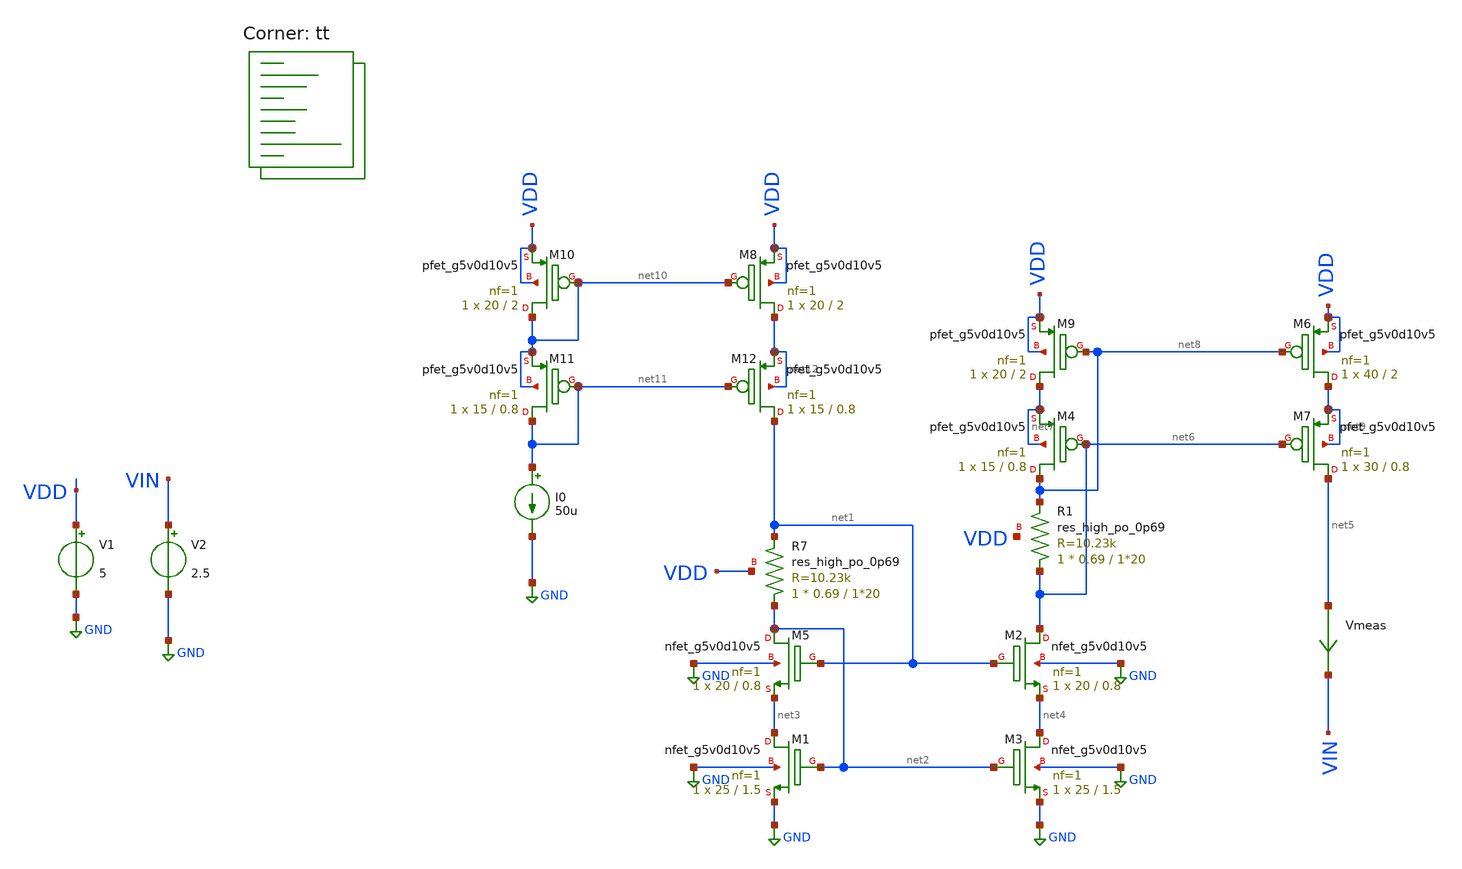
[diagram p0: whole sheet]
** sch_path: old stuff/folded_cascode_amplifier_upgraded/Low_voltage_current_mirror_NMOS/circ_test.sch
**.subckt circ_test
V1 VDD GND 5
V2 VIN GND 2.5
XR7 net2 net1 VDD sky130_fd_pr__res_high_po_0p69 L=1*20 mult=1 m=1
XM5 net2 net1 net3 GND sky130_fd_pr__nfet_g5v0d10v5 L=0.8 W=20 nf=1 ad='int((1 + 1)/2) * 20 / 1 * 0.29'
+ as='int((1 + 2)/2) * 20 / 1 * 0.29' pd='2*int((1 + 1)/2) * (20 / 1 + 0.29)' ps='2*int((1 + 2)/2) * (20 / 1 + 0.29)'
+ nrd='0.29 / 20 ' nrs='0.29 / 20 ' sa=0 sb=0 sd=0 mult=1 m=1
XM1 net3 net2 GND GND sky130_fd_pr__nfet_g5v0d10v5 L=1.5 W=25 nf=1 ad='int((1 + 1)/2) * 25 / 1 * 0.29'
+ as='int((1 + 2)/2) * 25 / 1 * 0.29' pd='2*int((1 + 1)/2) * (25 / 1 + 0.29)' ps='2*int((1 + 2)/2) * (25 / 1 + 0.29)'
+ nrd='0.29 / 25 ' nrs='0.29 / 25 ' sa=0 sb=0 sd=0 mult=1 m=1
I0 net11 GND 50u
XM3 net4 net2 GND GND sky130_fd_pr__nfet_g5v0d10v5 L=1.5 W=25 nf=1 ad='int((1 + 1)/2) * 25 / 1 * 0.29'
+ as='int((1 + 2)/2) * 25 / 1 * 0.29' pd='2*int((1 + 1)/2) * (25 / 1 + 0.29)' ps='2*int((1 + 2)/2) * (25 / 1 + 0.29)'
+ nrd='0.29 / 25 ' nrs='0.29 / 25 ' sa=0 sb=0 sd=0 mult=1 m=1
Vmeas net5 VIN 0
.save i(vmeas)
XM2 net6 net1 net4 GND sky130_fd_pr__nfet_g5v0d10v5 L=0.8 W=20 nf=1 ad='int((1 + 1)/2) * 20 / 1 * 0.29'
+ as='int((1 + 2)/2) * 20 / 1 * 0.29' pd='2*int((1 + 1)/2) * (20 / 1 + 0.29)' ps='2*int((1 + 2)/2) * (20 / 1 + 0.29)'
+ nrd='0.29 / 20 ' nrs='0.29 / 20 ' sa=0 sb=0 sd=0 mult=1 m=1
XM9 net7 net8 VDD VDD sky130_fd_pr__pfet_g5v0d10v5 L=2 W=20 nf=1 ad='int((1 + 1)/2) * 20 / 1 * 0.29'
+ as='int((1 + 2)/2) * 20 / 1 * 0.29' pd='2*int((1 + 1)/2) * (20 / 1 + 0.29)' ps='2*int((1 + 2)/2) * (20 / 1 + 0.29)'
+ nrd='0.29 / 20 ' nrs='0.29 / 20 ' sa=0 sb=0 sd=0 mult=1 m=1
XM4 net8 net6 net7 net7 sky130_fd_pr__pfet_g5v0d10v5 L=0.8 W=15 nf=1 ad='int((1 + 1)/2) * 15 / 1 * 0.29'
+ as='int((1 + 2)/2) * 15 / 1 * 0.29' pd='2*int((1 + 1)/2) * (15 / 1 + 0.29)' ps='2*int((1 + 2)/2) * (15 / 1 + 0.29)'
+ nrd='0.29 / 15 ' nrs='0.29 / 15 ' sa=0 sb=0 sd=0 mult=1 m=1
XR1 net6 net8 VDD sky130_fd_pr__res_high_po_0p69 L=1*20 mult=1 m=1
XM6 net9 net8 VDD VDD sky130_fd_pr__pfet_g5v0d10v5 L=2 W=40 nf=1 ad='int((1 + 1)/2) * 40 / 1 * 0.29'
+ as='int((1 + 2)/2) * 40 / 1 * 0.29' pd='2*int((1 + 1)/2) * (40 / 1 + 0.29)' ps='2*int((1 + 2)/2) * (40 / 1 + 0.29)'
+ nrd='0.29 / 40 ' nrs='0.29 / 40 ' sa=0 sb=0 sd=0 mult=1 m=1
XM7 net5 net6 net9 net9 sky130_fd_pr__pfet_g5v0d10v5 L=0.8 W=30 nf=1 ad='int((1 + 1)/2) * 30 / 1 * 0.29'
+ as='int((1 + 2)/2) * 30 / 1 * 0.29' pd='2*int((1 + 1)/2) * (30 / 1 + 0.29)' ps='2*int((1 + 2)/2) * (30 / 1 + 0.29)'
+ nrd='0.29 / 30 ' nrs='0.29 / 30 ' sa=0 sb=0 sd=0 mult=1 m=1
XM8 net12 net10 VDD VDD sky130_fd_pr__pfet_g5v0d10v5 L=2 W=20 nf=1 ad='int((1 + 1)/2) * 20 / 1 * 0.29'
+ as='int((1 + 2)/2) * 20 / 1 * 0.29' pd='2*int((1 + 1)/2) * (20 / 1 + 0.29)' ps='2*int((1 + 2)/2) * (20 / 1 + 0.29)'
+ nrd='0.29 / 20 ' nrs='0.29 / 20 ' sa=0 sb=0 sd=0 mult=1 m=1
XM10 net10 net10 VDD VDD sky130_fd_pr__pfet_g5v0d10v5 L=2 W=20 nf=1 ad='int((1 + 1)/2) * 20 / 1 * 0.29'
+ as='int((1 + 2)/2) * 20 / 1 * 0.29' pd='2*int((1 + 1)/2) * (20 / 1 + 0.29)' ps='2*int((1 + 2)/2) * (20 / 1 + 0.29)'
+ nrd='0.29 / 20 ' nrs='0.29 / 20 ' sa=0 sb=0 sd=0 mult=1 m=1
XM11 net11 net11 net10 net10 sky130_fd_pr__pfet_g5v0d10v5 L=0.8 W=15 nf=1 ad='int((1 + 1)/2) * 15 / 1 * 0.29'
+ as='int((1 + 2)/2) * 15 / 1 * 0.29' pd='2*int((1 + 1)/2) * (15 / 1 + 0.29)' ps='2*int((1 + 2)/2) * (15 / 1 + 0.29)'
+ nrd='0.29 / 15 ' nrs='0.29 / 15 ' sa=0 sb=0 sd=0 mult=1 m=1
XM12 net1 net11 net12 net12 sky130_fd_pr__pfet_g5v0d10v5 L=0.8 W=15 nf=1 ad='int((1 + 1)/2) * 15 / 1 * 0.29'
+ as='int((1 + 2)/2) * 15 / 1 * 0.29' pd='2*int((1 + 1)/2) * (15 / 1 + 0.29)' ps='2*int((1 + 2)/2) * (15 / 1 + 0.29)'
+ nrd='0.29 / 15 ' nrs='0.29 / 15 ' sa=0 sb=0 sd=0 mult=1 m=1
**** begin user architecture code

**************************************************************
**************************************************************
**************************************************************
**************************************************************
**************************************************************
*LIBs*********************************************************
**************************************************************
**************************************************************
**************************************************************
**************************************************************
**************************************************************
*.lib $::SKYWATER_MODELS/sky130.lib.spice tt
* chose the corners in the corner file
* tt_mm for mismatch
* ss ff sf fs standart corners
* ll hh lh hl capacitor and resistors corners
* mc for total process variation including corners
**************************************************************
**************************************************************
**************************************************************
**************************************************************
**************************************************************
*Corners/montecarlo options***********************************
**************************************************************
**************************************************************
**************************************************************
**************************************************************
**************************************************************
.TEMP 27
**************************************************************
**************************************************************
**************************************************************
**************************************************************
*SIMULATION and Plots*****************************************
**************************************************************
**************************************************************
**************************************************************
**************************************************************
.control
save all
dc V2 0 5 0.001
plot i(VMEAS)
plot (1/deriv(i(VMEAS)))
.endc

.lib $::SKYWATER_MODELS/sky130.lib.spice tt
**** end user architecture code
**.ends
.GLOBAL GND
.end
